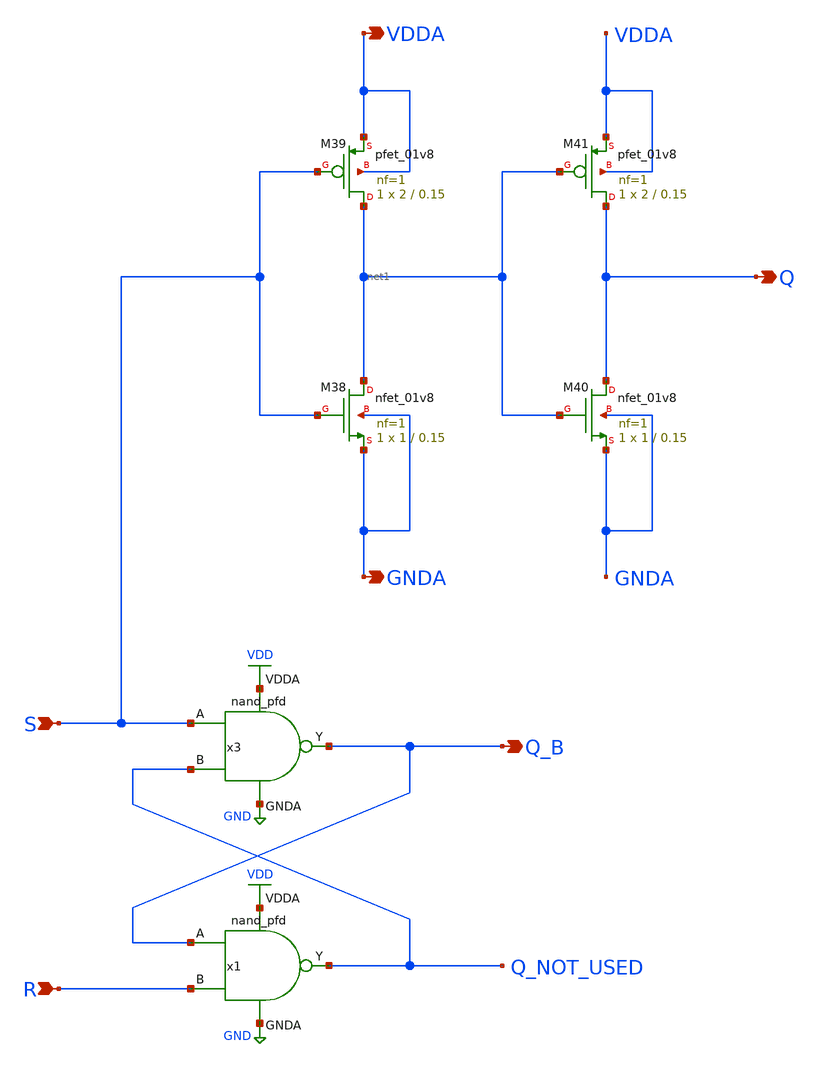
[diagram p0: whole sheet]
** sch_path: projects/ASU/EEE572/schematic/SR_latch.sch
**.subckt SR_latch S R Q Q_B GNDA VDDA
*.ipin S
*.ipin R
*.opin Q
*.opin Q_B
*.opin GNDA
*.opin VDDA
x3 VDD GND S Q_NOT_USED Q_B nand_pfd
x1 VDD GND Q_B R Q_NOT_USED nand_pfd
XM38 net1 S GNDA GNDA sky130_fd_pr__nfet_01v8 L=0.15 W=1 nf=1 ad='int((nf+1)/2) * W/nf * 0.29' as='int((nf+2)/2) * W/nf * 0.29'
+ pd='2*int((nf+1)/2) * (W/nf + 0.29)' ps='2*int((nf+2)/2) * (W/nf + 0.29)' nrd='0.29 / W' nrs='0.29 / W'
+ sa=0 sb=0 sd=0 mult=1 m=1
XM39 net1 S VDDA VDDA sky130_fd_pr__pfet_01v8 L=0.15 W=2 nf=1 ad='int((nf+1)/2) * W/nf * 0.29' as='int((nf+2)/2) * W/nf * 0.29'
+ pd='2*int((nf+1)/2) * (W/nf + 0.29)' ps='2*int((nf+2)/2) * (W/nf + 0.29)' nrd='0.29 / W' nrs='0.29 / W'
+ sa=0 sb=0 sd=0 mult=1 m=1
XM40 Q net1 GNDA GNDA sky130_fd_pr__nfet_01v8 L=0.15 W=1 nf=1 ad='int((nf+1)/2) * W/nf * 0.29' as='int((nf+2)/2) * W/nf * 0.29'
+ pd='2*int((nf+1)/2) * (W/nf + 0.29)' ps='2*int((nf+2)/2) * (W/nf + 0.29)' nrd='0.29 / W' nrs='0.29 / W'
+ sa=0 sb=0 sd=0 mult=1 m=1
XM41 Q net1 VDDA VDDA sky130_fd_pr__pfet_01v8 L=0.15 W=2 nf=1 ad='int((nf+1)/2) * W/nf * 0.29' as='int((nf+2)/2) * W/nf * 0.29'
+ pd='2*int((nf+1)/2) * (W/nf + 0.29)' ps='2*int((nf+2)/2) * (W/nf + 0.29)' nrd='0.29 / W' nrs='0.29 / W'
+ sa=0 sb=0 sd=0 mult=1 m=1
**.ends

* expanding   symbol:  nand_pfd.sym # of pins=5
** sym_path: projects/pll/pfd/xschem_ngspice/nand_pfd.sym
** sch_path: projects/pll/pfd/xschem_ngspice/nand_pfd.sch
.subckt nand_pfd VDDA GNDA A B Y
*.ipin A
*.opin Y
*.ipin VDDA
*.ipin GNDA
*.ipin B
XM4 Y B VDDA VDDA sky130_fd_pr__pfet_01v8 L=0.15 W=1 nf=2 ad='int((nf+1)/2) * W/nf * 0.29' as='int((nf+2)/2) * W/nf * 0.29'
+ pd='2*int((nf+1)/2) * (W/nf + 0.29)' ps='2*int((nf+2)/2) * (W/nf + 0.29)' nrd='0.29 / W' nrs='0.29 / W'
+ sa=0 sb=0 sd=0 mult=1 m=1
XM2 net1 B Y GNDA sky130_fd_pr__nfet_01v8 L=0.15 W=0.5 nf=1 ad='int((nf+1)/2) * W/nf * 0.29' as='int((nf+2)/2) * W/nf * 0.29'
+ pd='2*int((nf+1)/2) * (W/nf + 0.29)' ps='2*int((nf+2)/2) * (W/nf + 0.29)' nrd='0.29 / W' nrs='0.29 / W'
+ sa=0 sb=0 sd=0 mult=1 m=1
XM1 GNDA A net1 GNDA sky130_fd_pr__nfet_01v8 L=0.15 W=0.5 nf=1 ad='int((nf+1)/2) * W/nf * 0.29' as='int((nf+2)/2) * W/nf * 0.29'
+ pd='2*int((nf+1)/2) * (W/nf + 0.29)' ps='2*int((nf+2)/2) * (W/nf + 0.29)' nrd='0.29 / W' nrs='0.29 / W'
+ sa=0 sb=0 sd=0 mult=1 m=1
XM3 Y A VDDA VDDA sky130_fd_pr__pfet_01v8 L=0.15 W=1 nf=2 ad='int((nf+1)/2) * W/nf * 0.29' as='int((nf+2)/2) * W/nf * 0.29'
+ pd='2*int((nf+1)/2) * (W/nf + 0.29)' ps='2*int((nf+2)/2) * (W/nf + 0.29)' nrd='0.29 / W' nrs='0.29 / W'
+ sa=0 sb=0 sd=0 mult=1 m=1
.ends

.GLOBAL VDD
.GLOBAL GND
.end
